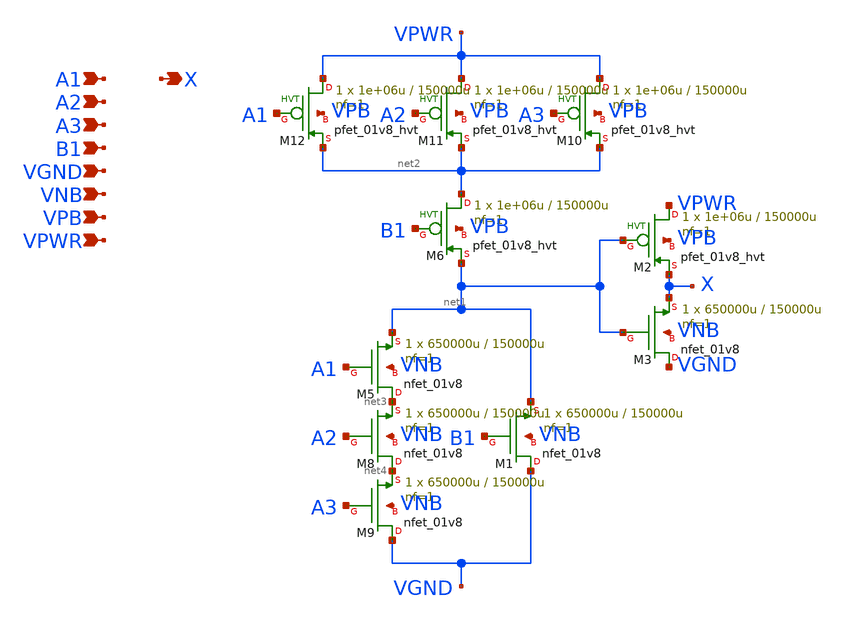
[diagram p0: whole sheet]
** sch_path: schematics/a31o/sky130_fd_sc_hd__a31o_1.sch
**.subckt sky130_fd_sc_hd__a31o_1 A1 A2 A3 B1 VGND VNB VPB VPWR X
*.ipin A1
*.ipin A2
*.ipin A3
*.ipin B1
*.ipin VGND
*.ipin VNB
*.ipin VPB
*.ipin VPWR
*.opin X
XM1 VGND B1 net1 VNB sky130_fd_pr__nfet_01v8 L=150000u W=650000u nf=1 ad='int((1 + 1)/2) * 650000u / 1 * 0.29'
+ as='int((1 + 2)/2) * 650000u / 1 * 0.29' pd='2*int((1 + 1)/2) * (650000u / 1 + 0.29)' ps='2*int((1 + 2)/2) * (650000u / 1 + 0.29)'
+ nrd='0.29 / 650000u ' nrs='0.29 / 650000u ' sa=0 sb=0 sd=0 mult=1 m=1
XM2 VPWR net1 X VPB sky130_fd_pr__pfet_01v8_hvt L=150000u W=1e+06u nf=1 ad='int((1 + 1)/2) * 1e+06u / 1 * 0.29'
+ as='int((1 + 2)/2) * 1e+06u / 1 * 0.29' pd='2*int((1 + 1)/2) * (1e+06u / 1 + 0.29)' ps='2*int((1 + 2)/2) * (1e+06u / 1 + 0.29)'
+ nrd='0.29 / 1e+06u ' nrs='0.29 / 1e+06u ' sa=0 sb=0 sd=0 mult=1 m=1
XM3 VGND net1 X VNB sky130_fd_pr__nfet_01v8 L=150000u W=650000u nf=1 ad='int((1 + 1)/2) * 650000u / 1 * 0.29'
+ as='int((1 + 2)/2) * 650000u / 1 * 0.29' pd='2*int((1 + 1)/2) * (650000u / 1 + 0.29)' ps='2*int((1 + 2)/2) * (650000u / 1 + 0.29)'
+ nrd='0.29 / 650000u ' nrs='0.29 / 650000u ' sa=0 sb=0 sd=0 mult=1 m=1
XM5 net3 A1 net1 VNB sky130_fd_pr__nfet_01v8 L=150000u W=650000u nf=1 ad='int((1 + 1)/2) * 650000u / 1 * 0.29'
+ as='int((1 + 2)/2) * 650000u / 1 * 0.29' pd='2*int((1 + 1)/2) * (650000u / 1 + 0.29)' ps='2*int((1 + 2)/2) * (650000u / 1 + 0.29)'
+ nrd='0.29 / 650000u ' nrs='0.29 / 650000u ' sa=0 sb=0 sd=0 mult=1 m=1
XM6 net2 B1 net1 VPB sky130_fd_pr__pfet_01v8_hvt L=150000u W=1e+06u nf=1 ad='int((1 + 1)/2) * 1e+06u / 1 * 0.29'
+ as='int((1 + 2)/2) * 1e+06u / 1 * 0.29' pd='2*int((1 + 1)/2) * (1e+06u / 1 + 0.29)' ps='2*int((1 + 2)/2) * (1e+06u / 1 + 0.29)'
+ nrd='0.29 / 1e+06u ' nrs='0.29 / 1e+06u ' sa=0 sb=0 sd=0 mult=1 m=1
XM8 net4 A2 net3 VNB sky130_fd_pr__nfet_01v8 L=150000u W=650000u nf=1 ad='int((1 + 1)/2) * 650000u / 1 * 0.29'
+ as='int((1 + 2)/2) * 650000u / 1 * 0.29' pd='2*int((1 + 1)/2) * (650000u / 1 + 0.29)' ps='2*int((1 + 2)/2) * (650000u / 1 + 0.29)'
+ nrd='0.29 / 650000u ' nrs='0.29 / 650000u ' sa=0 sb=0 sd=0 mult=1 m=1
XM9 VGND A3 net4 VNB sky130_fd_pr__nfet_01v8 L=150000u W=650000u nf=1 ad='int((1 + 1)/2) * 650000u / 1 * 0.29'
+ as='int((1 + 2)/2) * 650000u / 1 * 0.29' pd='2*int((1 + 1)/2) * (650000u / 1 + 0.29)' ps='2*int((1 + 2)/2) * (650000u / 1 + 0.29)'
+ nrd='0.29 / 650000u ' nrs='0.29 / 650000u ' sa=0 sb=0 sd=0 mult=1 m=1
XM10 VPWR A3 net2 VPB sky130_fd_pr__pfet_01v8_hvt L=150000u W=1e+06u nf=1 ad='int((1 + 1)/2) * 1e+06u / 1 * 0.29'
+ as='int((1 + 2)/2) * 1e+06u / 1 * 0.29' pd='2*int((1 + 1)/2) * (1e+06u / 1 + 0.29)' ps='2*int((1 + 2)/2) * (1e+06u / 1 + 0.29)'
+ nrd='0.29 / 1e+06u ' nrs='0.29 / 1e+06u ' sa=0 sb=0 sd=0 mult=1 m=1
XM11 VPWR A2 net2 VPB sky130_fd_pr__pfet_01v8_hvt L=150000u W=1e+06u nf=1 ad='int((1 + 1)/2) * 1e+06u / 1 * 0.29'
+ as='int((1 + 2)/2) * 1e+06u / 1 * 0.29' pd='2*int((1 + 1)/2) * (1e+06u / 1 + 0.29)' ps='2*int((1 + 2)/2) * (1e+06u / 1 + 0.29)'
+ nrd='0.29 / 1e+06u ' nrs='0.29 / 1e+06u ' sa=0 sb=0 sd=0 mult=1 m=1
XM12 VPWR A1 net2 VPB sky130_fd_pr__pfet_01v8_hvt L=150000u W=1e+06u nf=1 ad='int((1 + 1)/2) * 1e+06u / 1 * 0.29'
+ as='int((1 + 2)/2) * 1e+06u / 1 * 0.29' pd='2*int((1 + 1)/2) * (1e+06u / 1 + 0.29)' ps='2*int((1 + 2)/2) * (1e+06u / 1 + 0.29)'
+ nrd='0.29 / 1e+06u ' nrs='0.29 / 1e+06u ' sa=0 sb=0 sd=0 mult=1 m=1
**.ends
.end
